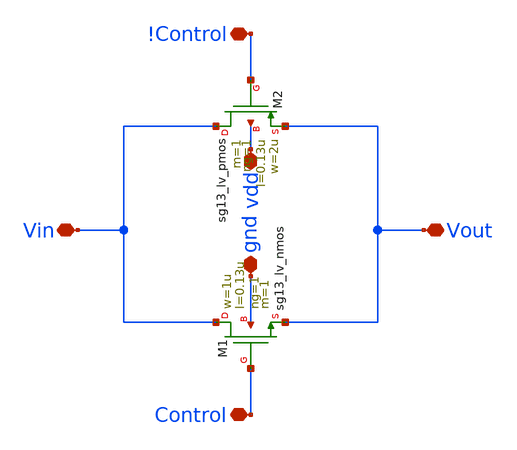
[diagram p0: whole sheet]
** sch_path: modules/module_3_8_bit_SAR_ADC/part_2_digital_comps/T_gate/schematic/T_gate.sch
**.subckt T_gate Vout Vin !Control Control gnd vdd
*.iopin Vout
*.iopin Vin
*.iopin !Control
*.iopin Control
*.iopin gnd
*.iopin vdd
XM1 Vin Control Vout gnd sg13_lv_nmos w=1u l=0.13u ng=1 m=1 mm_ok=1
XM2 Vin !Control Vout vdd sg13_lv_pmos w=2u l=0.13u ng=1 m=1 mm_ok=1
**.ends
.end
